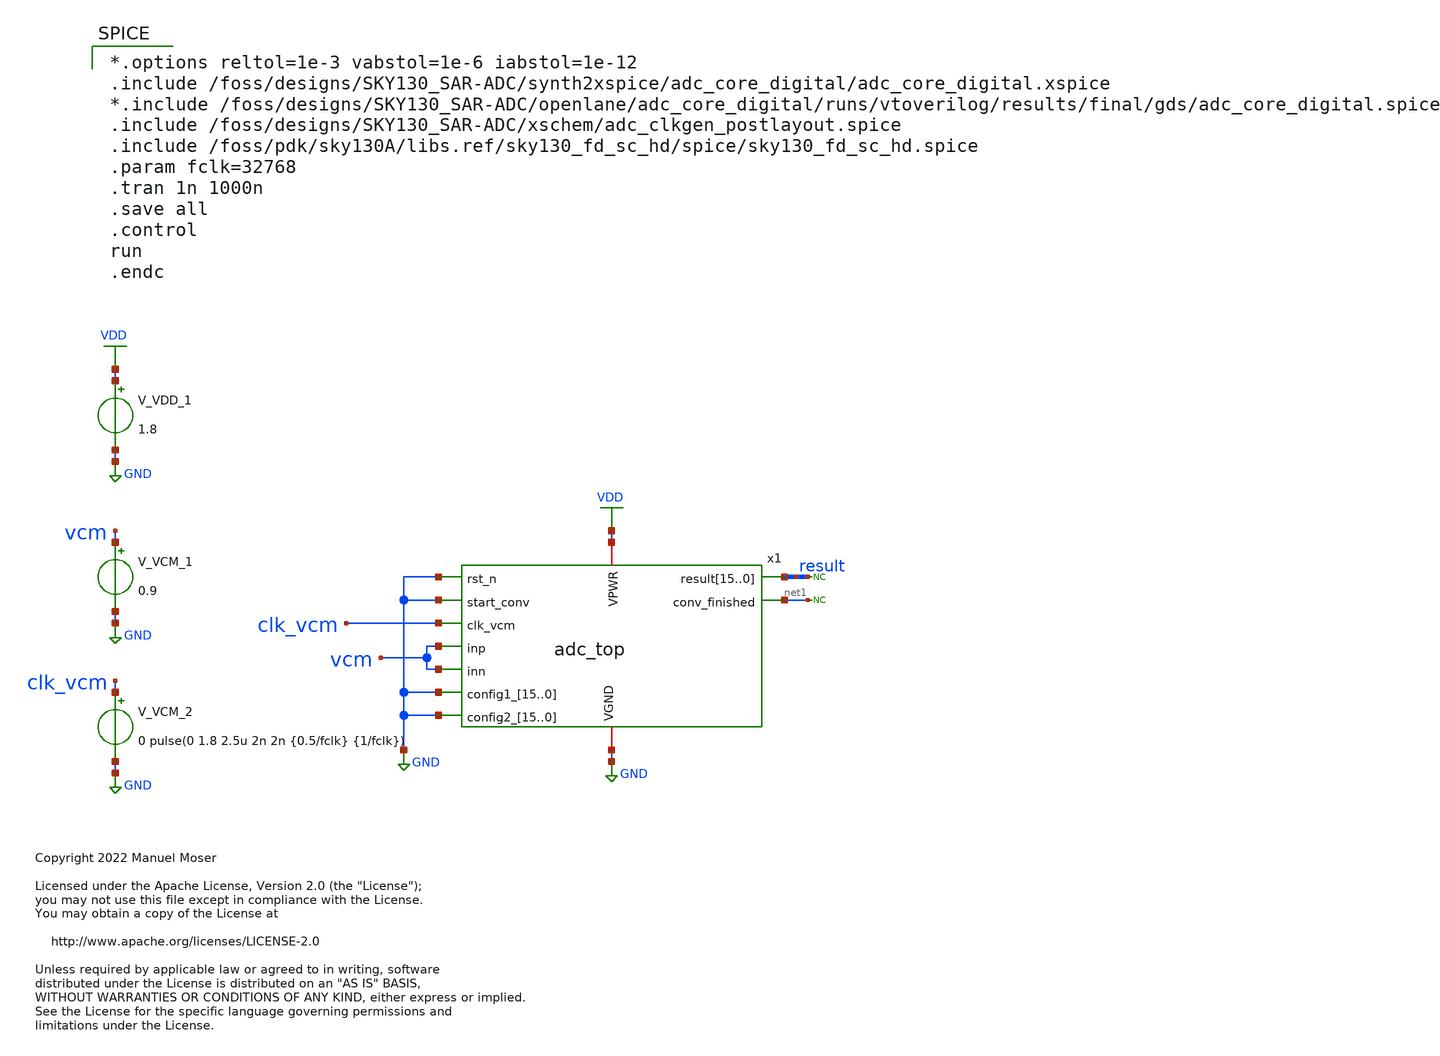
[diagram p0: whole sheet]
** sch_path: xschem/adc_top_tb.sch
* Copyright 2022 Manuel Moser
* Licensed under the Apache License, Version 2.0 (the "License");
**.subckt adc_top_tb
x1 result result result result result result result result result result result result result result
+ result result VDD GND net1 GND GND clk_vcm vcm vcm GND GND GND GND GND GND GND GND GND GND GND GND GND GND
+ GND GND GND GND GND GND GND GND GND GND GND GND GND GND GND GND GND GND adc_top
V_VDD_1 VDD GND 1.8
V_VCM_1 vcm GND 0.9
V_VCM_2 clk_vcm GND 0 pulse(0 1.8 2.5u 2n 2n {0.5/fclk} {1/fclk})
* noconn result
* noconn #net1
**** begin user architecture code

*.options reltol=1e-3 vabstol=1e-6 iabstol=1e-12
.include /foss/designs/SKY130_SAR-ADC/synth2xspice/adc_core_digital/adc_core_digital.xspice
*.include /foss/designs/SKY130_SAR-ADC/openlane/adc_core_digital/runs/vtoverilog/results/final/gds/adc_core_digital.spice
.include /foss/designs/SKY130_SAR-ADC/xschem/adc_clkgen_postlayout.spice
.include /foss/pdk/sky130A/libs.ref/sky130_fd_sc_hd/spice/sky130_fd_sc_hd.spice
.param fclk=32768
.tran 1n 1000n
.save all
.control
run
.endc



** opencircuitdesign pdks install
.lib $::SKYWATER_MODELS/sky130.lib.spice tt


**** end user architecture code
**.ends
.GLOBAL VDD
.GLOBAL GND
.end
